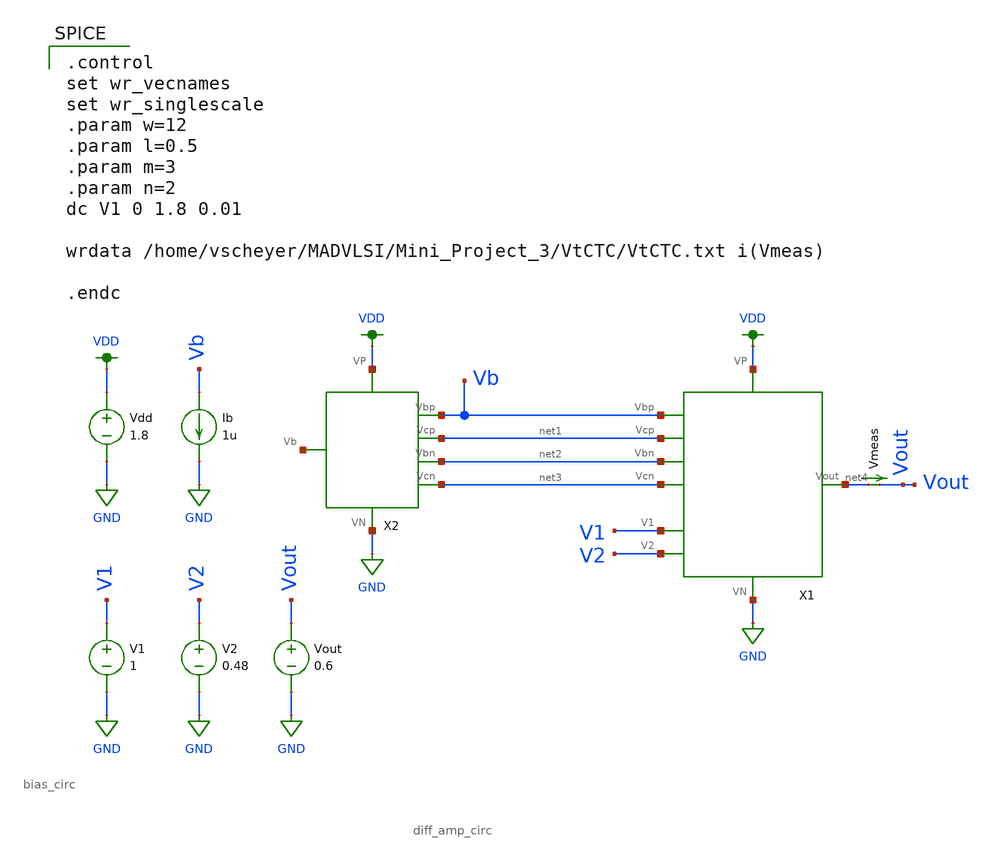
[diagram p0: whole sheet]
** sch_path: Mini_Project_3/diff_amp_VtCTC.sch
**.subckt diff_amp_VtCTC
X2 VDD GND net3 net2 net1 Vb net5 bias_circ
Vdd VDD GND 1.8
Ib Vb GND 1u
V1 V1 GND 1
V2 V2 GND 0.48
Vmeas net4 Vout 0
.save i(vmeas)
Vout Vout GND 0.6
X1 Vb net1 net2 net3 net4 GND VDD V1 V2 diff_amp_circ
**** begin user architecture code

.option wnflag=1
.lib ~/skywater/skywater-pdk/libraries/sky130_fd_pr_ngspice/latest/models/sky130.lib.spice tt


.control
set wr_vecnames
set wr_singlescale
.param w=12
.param l=0.5
.param m=3
.param n=2
dc V1 0 1.8 0.01

wrdata /home/vscheyer/MADVLSI/Mini_Project_3/VtCTC/VtCTC.txt i(Vmeas)

.endc

**** end user architecture code
**.ends
.GLOBAL VDD
.GLOBAL GND
.end
